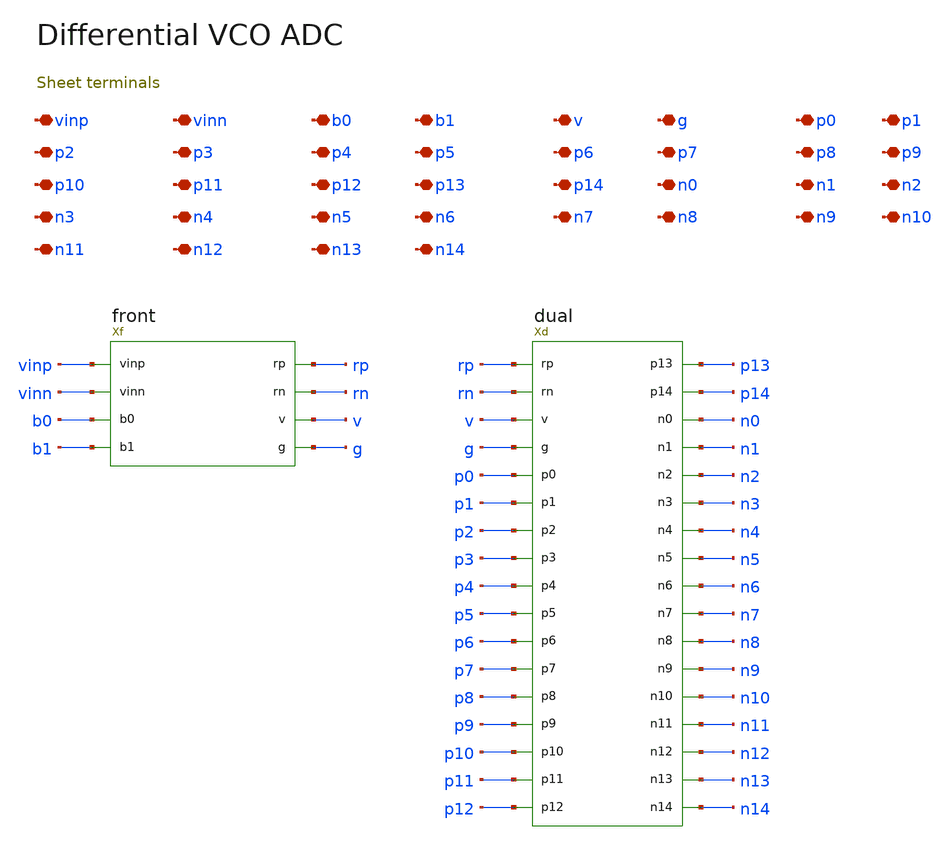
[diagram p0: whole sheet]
** sch_path: review/xschem/adc_analog.sch
**.subckt adc_analog vinp vinn b0 b1 v g p0 p1 p2 p3 p4 p5 p6 p7 p8 p9 p10 p11 p12 p13 p14 n0 n1 n2
*+ n3 n4 n5 n6 n7 n8 n9 n10 n11 n12 n13 n14
*.iopin vinp
*.iopin vinn
*.iopin b0
*.iopin b1
*.iopin v
*.iopin g
*.iopin p0
*.iopin p1
*.iopin p2
*.iopin p3
*.iopin p4
*.iopin p5
*.iopin p6
*.iopin p7
*.iopin p8
*.iopin p9
*.iopin p10
*.iopin p11
*.iopin p12
*.iopin p13
*.iopin p14
*.iopin n0
*.iopin n1
*.iopin n2
*.iopin n3
*.iopin n4
*.iopin n5
*.iopin n6
*.iopin n7
*.iopin n8
*.iopin n9
*.iopin n10
*.iopin n11
*.iopin n12
*.iopin n13
*.iopin n14
Xf vinp vinn b0 b1 rp rn v g front
Xd rp rn v g p0 p1 p2 p3 p4 p5 p6 p7 p8 p9 p10 p11 p12 p13 p14 n0 n1 n2 n3 n4 n5 n6 n7 n8 n9 n10 n11
+ n12 n13 n14 dual
**.ends

* expanding   symbol:  front.sym # of pins=8
** sym_path: review/xschem/front.sym
** sch_path: review/xschem/front.sch
.subckt front vinp vinn b0 b1 rp rn v g
*.iopin vinp
*.iopin vinn
*.iopin b0
*.iopin b1
*.iopin rp
*.iopin rn
*.iopin v
*.iopin g
Xbias b0 b1 vb g4 g15 g20 v g bias
Xtailp sp vb g4 g15 g20 v tail
Xtailn sn vb g4 g15 g20 v tail
XMinp0 rp vinn sp sp sky130_fd_pr__pfet_01v8_lvt L=1 W=6 nf=1 ad='int((1 + 1)/2) * 6 / 1 * 0.29' as='int((1 + 2)/2) * 6 / 1 * 0.29'
+ pd='2*int((1 + 1)/2) * (6 / 1 + 0.29)' ps='2*int((1 + 2)/2) * (6 / 1 + 0.29)' nrd='0.29 / 6 ' nrs='0.29 / 6 '
+ sa=0 sb=0 sd=0 mult=1 m=1
XMinp1 rp vinn sp sp sky130_fd_pr__pfet_01v8_lvt L=1 W=6 nf=1 ad='int((1 + 1)/2) * 6 / 1 * 0.29' as='int((1 + 2)/2) * 6 / 1 * 0.29'
+ pd='2*int((1 + 1)/2) * (6 / 1 + 0.29)' ps='2*int((1 + 2)/2) * (6 / 1 + 0.29)' nrd='0.29 / 6 ' nrs='0.29 / 6 '
+ sa=0 sb=0 sd=0 mult=1 m=1
XMinp2 rp vinn sp sp sky130_fd_pr__pfet_01v8_lvt L=1 W=6 nf=1 ad='int((1 + 1)/2) * 6 / 1 * 0.29' as='int((1 + 2)/2) * 6 / 1 * 0.29'
+ pd='2*int((1 + 1)/2) * (6 / 1 + 0.29)' ps='2*int((1 + 2)/2) * (6 / 1 + 0.29)' nrd='0.29 / 6 ' nrs='0.29 / 6 '
+ sa=0 sb=0 sd=0 mult=1 m=1
XMinp3 rp vinn sp sp sky130_fd_pr__pfet_01v8_lvt L=1 W=6 nf=1 ad='int((1 + 1)/2) * 6 / 1 * 0.29' as='int((1 + 2)/2) * 6 / 1 * 0.29'
+ pd='2*int((1 + 1)/2) * (6 / 1 + 0.29)' ps='2*int((1 + 2)/2) * (6 / 1 + 0.29)' nrd='0.29 / 6 ' nrs='0.29 / 6 '
+ sa=0 sb=0 sd=0 mult=1 m=1
XMinn0 rn vinp sn sn sky130_fd_pr__pfet_01v8_lvt L=1 W=6 nf=1 ad='int((1 + 1)/2) * 6 / 1 * 0.29' as='int((1 + 2)/2) * 6 / 1 * 0.29'
+ pd='2*int((1 + 1)/2) * (6 / 1 + 0.29)' ps='2*int((1 + 2)/2) * (6 / 1 + 0.29)' nrd='0.29 / 6 ' nrs='0.29 / 6 '
+ sa=0 sb=0 sd=0 mult=1 m=1
XMinn1 rn vinp sn sn sky130_fd_pr__pfet_01v8_lvt L=1 W=6 nf=1 ad='int((1 + 1)/2) * 6 / 1 * 0.29' as='int((1 + 2)/2) * 6 / 1 * 0.29'
+ pd='2*int((1 + 1)/2) * (6 / 1 + 0.29)' ps='2*int((1 + 2)/2) * (6 / 1 + 0.29)' nrd='0.29 / 6 ' nrs='0.29 / 6 '
+ sa=0 sb=0 sd=0 mult=1 m=1
XMinn2 rn vinp sn sn sky130_fd_pr__pfet_01v8_lvt L=1 W=6 nf=1 ad='int((1 + 1)/2) * 6 / 1 * 0.29' as='int((1 + 2)/2) * 6 / 1 * 0.29'
+ pd='2*int((1 + 1)/2) * (6 / 1 + 0.29)' ps='2*int((1 + 2)/2) * (6 / 1 + 0.29)' nrd='0.29 / 6 ' nrs='0.29 / 6 '
+ sa=0 sb=0 sd=0 mult=1 m=1
XMinn3 rn vinp sn sn sky130_fd_pr__pfet_01v8_lvt L=1 W=6 nf=1 ad='int((1 + 1)/2) * 6 / 1 * 0.29' as='int((1 + 2)/2) * 6 / 1 * 0.29'
+ pd='2*int((1 + 1)/2) * (6 / 1 + 0.29)' ps='2*int((1 + 2)/2) * (6 / 1 + 0.29)' nrd='0.29 / 6 ' nrs='0.29 / 6 '
+ sa=0 sb=0 sd=0 mult=1 m=1
XRr0 sp mid g sky130_fd_pr__res_high_po_0p69 L=80 mult=1 m=1
XRr1 mid sn g sky130_fd_pr__res_high_po_0p69 L=80 mult=1 m=1
XCcapP rp g sky130_fd_pr__cap_mim_m3_1 W=21.8 L=21.8 MF=1 m=1
XCcapN rn g sky130_fd_pr__cap_mim_m3_1 W=21.8 L=21.8 MF=1 m=1
.ends


* expanding   symbol:  dual.sym # of pins=34
** sym_path: review/xschem/dual.sym
** sch_path: review/xschem/dual.sch
.subckt dual rp rn v g p0 p1 p2 p3 p4 p5 p6 p7 p8 p9 p10 p11 p12 p13 p14 n0 n1 n2 n3 n4 n5 n6 n7 n8
+ n9 n10 n11 n12 n13 n14
*.iopin rp
*.iopin rn
*.iopin v
*.iopin g
*.iopin p0
*.iopin p1
*.iopin p2
*.iopin p3
*.iopin p4
*.iopin p5
*.iopin p6
*.iopin p7
*.iopin p8
*.iopin p9
*.iopin p10
*.iopin p11
*.iopin p12
*.iopin p13
*.iopin p14
*.iopin n0
*.iopin n1
*.iopin n2
*.iopin n3
*.iopin n4
*.iopin n5
*.iopin n6
*.iopin n7
*.iopin n8
*.iopin n9
*.iopin n10
*.iopin n11
*.iopin n12
*.iopin n13
*.iopin n14
Xp rp v g p0 p1 p2 p3 p4 p5 p6 p7 p8 p9 p10 p11 p12 p13 p14 ring
Xn rn v g n0 n1 n2 n3 n4 n5 n6 n7 n8 n9 n10 n11 n12 n13 n14 ring
.ends


* expanding   symbol:  bias.sym # of pins=8
** sym_path: review/xschem/bias.sym
** sch_path: review/xschem/bias.sch
.subckt bias b0 b1 vb g4 g15 g20 v g
*.iopin b0
*.iopin b1
*.iopin vb
*.iopin g4
*.iopin g15
*.iopin g20
*.iopin v
*.iopin g
Xreference vb v g beta_ref
XMi0p nb0 b0 v v sky130_fd_pr__pfet_01v8 L=.15 W=.84 nf=1 ad='int((nf+1)/2) * W/nf * 0.29' as='int((nf+2)/2) * W/nf * 0.29'
+ pd='2*int((nf+1)/2) * (W/nf + 0.29)' ps='2*int((nf+2)/2) * (W/nf + 0.29)' nrd='0.29 / W' nrs='0.29 / W'
+ sa=0 sb=0 sd=0 mult=1 m=1
XMi0n nb0 b0 g g sky130_fd_pr__nfet_01v8 L=.15 W=.42 nf=1 ad='int((1 + 1)/2) * .42 / 1 * 0.29' as='int((1 + 2)/2) * .42 / 1 * 0.29'
+ pd='2*int((1 + 1)/2) * (.42 / 1 + 0.29)' ps='2*int((1 + 2)/2) * (.42 / 1 + 0.29)' nrd='0.29 / .42 ' nrs='0.29 / .42 '
+ sa=0 sb=0 sd=0 mult=1 m=1
XMi1p nb1 b1 v v sky130_fd_pr__pfet_01v8 L=.15 W=.84 nf=1 ad='int((nf+1)/2) * W/nf * 0.29' as='int((nf+2)/2) * W/nf * 0.29'
+ pd='2*int((nf+1)/2) * (W/nf + 0.29)' ps='2*int((nf+2)/2) * (W/nf + 0.29)' nrd='0.29 / W' nrs='0.29 / W'
+ sa=0 sb=0 sd=0 mult=1 m=1
XMi1n nb1 b1 g g sky130_fd_pr__nfet_01v8 L=.15 W=.42 nf=1 ad='int((1 + 1)/2) * .42 / 1 * 0.29' as='int((1 + 2)/2) * .42 / 1 * 0.29'
+ pd='2*int((1 + 1)/2) * (.42 / 1 + 0.29)' ps='2*int((1 + 2)/2) * (.42 / 1 + 0.29)' nrd='0.29 / .42 ' nrs='0.29 / .42 '
+ sa=0 sb=0 sd=0 mult=1 m=1
Xonlylow nb0 b1 off4 v g nor2
XMi4p en4 off4 v v sky130_fd_pr__pfet_01v8 L=.15 W=.84 nf=1 ad='int((nf+1)/2) * W/nf * 0.29' as='int((nf+2)/2) * W/nf * 0.29'
+ pd='2*int((nf+1)/2) * (W/nf + 0.29)' ps='2*int((nf+2)/2) * (W/nf + 0.29)' nrd='0.29 / W' nrs='0.29 / W'
+ sa=0 sb=0 sd=0 mult=1 m=1
XMi4n en4 off4 g g sky130_fd_pr__nfet_01v8 L=.15 W=.42 nf=1 ad='int((1 + 1)/2) * .42 / 1 * 0.29' as='int((1 + 2)/2) * .42 / 1 * 0.29'
+ pd='2*int((1 + 1)/2) * (.42 / 1 + 0.29)' ps='2*int((1 + 2)/2) * (.42 / 1 + 0.29)' nrd='0.29 / .42 ' nrs='0.29 / .42 '
+ sa=0 sb=0 sd=0 mult=1 m=1
Xboth nb0 nb1 en20 v g nor2
Xzero b0 b1 zero v g nor2
Xdiff zero en20 off15 v g nor2
XMi15p en15 off15 v v sky130_fd_pr__pfet_01v8 L=.15 W=.84 nf=1 ad='int((nf+1)/2) * W/nf * 0.29' as='int((nf+2)/2) * W/nf * 0.29'
+ pd='2*int((nf+1)/2) * (W/nf + 0.29)' ps='2*int((nf+2)/2) * (W/nf + 0.29)' nrd='0.29 / W' nrs='0.29 / W'
+ sa=0 sb=0 sd=0 mult=1 m=1
XMi15n en15 off15 g g sky130_fd_pr__nfet_01v8 L=.15 W=.42 nf=1 ad='int((1 + 1)/2) * .42 / 1 * 0.29' as='int((1 + 2)/2) * .42 / 1 * 0.29'
+ pd='2*int((1 + 1)/2) * (.42 / 1 + 0.29)' ps='2*int((1 + 2)/2) * (.42 / 1 + 0.29)' nrd='0.29 / .42 ' nrs='0.29 / .42 '
+ sa=0 sb=0 sd=0 mult=1 m=1
XMi20p off20 en20 v v sky130_fd_pr__pfet_01v8 L=.15 W=.84 nf=1 ad='int((nf+1)/2) * W/nf * 0.29' as='int((nf+2)/2) * W/nf * 0.29'
+ pd='2*int((nf+1)/2) * (W/nf + 0.29)' ps='2*int((nf+2)/2) * (W/nf + 0.29)' nrd='0.29 / W' nrs='0.29 / W'
+ sa=0 sb=0 sd=0 mult=1 m=1
XMi20n off20 en20 g g sky130_fd_pr__nfet_01v8 L=.15 W=.42 nf=1 ad='int((1 + 1)/2) * .42 / 1 * 0.29' as='int((1 + 2)/2) * .42 / 1 * 0.29'
+ pd='2*int((1 + 1)/2) * (.42 / 1 + 0.29)' ps='2*int((1 + 2)/2) * (.42 / 1 + 0.29)' nrd='0.29 / .42 ' nrs='0.29 / .42 '
+ sa=0 sb=0 sd=0 mult=1 m=1
Xsw4 en4 off4 vb g4 v g tailgate
Xsw15 en15 off15 vb g15 v g tailgate
Xsw20 en20 off20 vb g20 v g tailgate
.ends


* expanding   symbol:  tail.sym # of pins=6
** sym_path: review/xschem/tail.sym
** sch_path: review/xschem/tail.sch
.subckt tail s vb g4 g15 g20 v
*.iopin s
*.iopin vb
*.iopin g4
*.iopin g15
*.iopin g20
*.iopin v
XMone s vb v v sky130_fd_pr__pfet_01v8 L=2 W=1 nf=1 ad='int((nf+1)/2) * W/nf * 0.29' as='int((nf+2)/2) * W/nf * 0.29'
+ pd='2*int((nf+1)/2) * (W/nf + 0.29)' ps='2*int((nf+2)/2) * (W/nf + 0.29)' nrd='0.29 / W' nrs='0.29 / W'
+ sa=0 sb=0 sd=0 mult=1 m=1
Xunits4 s g4 v units4
Xunits15 s g15 v units15
Xunits20 s g20 v units20
.ends


* expanding   symbol:  ring.sym # of pins=18
** sym_path: review/xschem/ring.sym
** sch_path: review/xschem/ring.sch
.subckt ring rail v g t0 t1 t2 t3 t4 t5 t6 t7 t8 t9 t10 t11 t12 t13 t14
*.iopin rail
*.iopin v
*.iopin g
*.iopin t0
*.iopin t1
*.iopin t2
*.iopin t3
*.iopin t4
*.iopin t5
*.iopin t6
*.iopin t7
*.iopin t8
*.iopin t9
*.iopin t10
*.iopin t11
*.iopin t12
*.iopin t13
*.iopin t14
Xbank rail v g oa0 ob0 oa1 ob1 oa2 ob2 oa3 ob3 oa4 ob4 oa5 ob5 oa6 ob6 oa7 ob7 oa8 ob8 oa9 ob9 oa10
+ ob10 oa11 ob11 oa12 ob12 oa13 ob13 oa14 ob14 bank
Xl0 oa0 ob0 t0 v g cvsl
Xl1 oa1 ob1 t1 v g cvsl
Xl2 oa2 ob2 t2 v g cvsl
Xl3 oa3 ob3 t3 v g cvsl
Xl4 oa4 ob4 t4 v g cvsl
Xl5 oa5 ob5 t5 v g cvsl
Xl6 oa6 ob6 t6 v g cvsl
Xl7 oa7 ob7 t7 v g cvsl
Xl8 oa8 ob8 t8 v g cvsl
Xl9 oa9 ob9 t9 v g cvsl
Xl10 oa10 ob10 t10 v g cvsl
Xl11 oa11 ob11 t11 v g cvsl
Xl12 oa12 ob12 t12 v g cvsl
Xl13 oa13 ob13 t13 v g cvsl
Xl14 oa14 ob14 t14 v g cvsl
.ends


* expanding   symbol:  beta_ref.sym # of pins=3
** sym_path: review/xschem/beta_ref.sym
** sch_path: review/xschem/beta_ref.sch
.subckt beta_ref vb v g
*.iopin vb
*.iopin v
*.iopin g
XMp0 vb vb v v sky130_fd_pr__pfet_01v8 L=2 W=2 nf=1 ad='int((nf+1)/2) * W/nf * 0.29' as='int((nf+2)/2) * W/nf * 0.29'
+ pd='2*int((nf+1)/2) * (W/nf + 0.29)' ps='2*int((nf+2)/2) * (W/nf + 0.29)' nrd='0.29 / W' nrs='0.29 / W'
+ sa=0 sb=0 sd=0 mult=1 m=1
XMn0 vn vn g g sky130_fd_pr__nfet_01v8 L=2 W=2 nf=1 ad='int((1 + 1)/2) * 2 / 1 * 0.29' as='int((1 + 2)/2) * 2 / 1 * 0.29'
+ pd='2*int((1 + 1)/2) * (2 / 1 + 0.29)' ps='2*int((1 + 2)/2) * (2 / 1 + 0.29)' nrd='0.29 / 2 ' nrs='0.29 / 2 '
+ sa=0 sb=0 sd=0 mult=1 m=1
XMp1 vn vb v v sky130_fd_pr__pfet_01v8 L=2 W=2 nf=1 ad='int((nf+1)/2) * W/nf * 0.29' as='int((nf+2)/2) * W/nf * 0.29'
+ pd='2*int((nf+1)/2) * (W/nf + 0.29)' ps='2*int((nf+2)/2) * (W/nf + 0.29)' nrd='0.29 / W' nrs='0.29 / W'
+ sa=0 sb=0 sd=0 mult=1 m=1
XMn1 vb vn rs g sky130_fd_pr__nfet_01v8 L=2 W=8 nf=1 ad='int((1 + 1)/2) * 8 / 1 * 0.29' as='int((1 + 2)/2) * 8 / 1 * 0.29'
+ pd='2*int((1 + 1)/2) * (8 / 1 + 0.29)' ps='2*int((1 + 2)/2) * (8 / 1 + 0.29)' nrd='0.29 / 8 ' nrs='0.29 / 8 '
+ sa=0 sb=0 sd=0 mult=1 m=1
XRref0 rs refmid g sky130_fd_pr__res_high_po_0p69 L=97.1 mult=1 m=1
XRref1 refmid g g sky130_fd_pr__res_high_po_0p69 L=97.1 mult=1 m=1
XMweak kick g v v sky130_fd_pr__pfet_01v8 L=12 W=.42 nf=1 ad='int((nf+1)/2) * W/nf * 0.29' as='int((nf+2)/2) * W/nf * 0.29'
+ pd='2*int((nf+1)/2) * (W/nf + 0.29)' ps='2*int((nf+2)/2) * (W/nf + 0.29)' nrd='0.29 / W' nrs='0.29 / W'
+ sa=0 sb=0 sd=0 mult=1 m=1
XMsense kick vn g g sky130_fd_pr__nfet_01v8_lvt L=.15 W=5 nf=1 ad='int((1 + 1)/2) * 5 / 1 * 0.29' as='int((1 + 2)/2) * 5 / 1 * 0.29'
+ pd='2*int((1 + 1)/2) * (5 / 1 + 0.29)' ps='2*int((1 + 2)/2) * (5 / 1 + 0.29)' nrd='0.29 / 5 ' nrs='0.29 / 5 '
+ sa=0 sb=0 sd=0 mult=1 m=1
XMkick vb kick g g sky130_fd_pr__nfet_01v8 L=1 W=.5 nf=1 ad='int((1 + 1)/2) * .5 / 1 * 0.29' as='int((1 + 2)/2) * .5 / 1 * 0.29'
+ pd='2*int((1 + 1)/2) * (.5 / 1 + 0.29)' ps='2*int((1 + 2)/2) * (.5 / 1 + 0.29)' nrd='0.29 / .5 ' nrs='0.29 / .5 '
+ sa=0 sb=0 sd=0 mult=1 m=1
.ends


* expanding   symbol:  nor2.sym # of pins=5
** sym_path: review/xschem/nor2.sym
** sch_path: review/xschem/nor2.sch
.subckt nor2 a b y v g
*.iopin a
*.iopin b
*.iopin y
*.iopin v
*.iopin g
XMp0 mid a v v sky130_fd_pr__pfet_01v8 L=.15 W=.84 nf=1 ad='int((nf+1)/2) * W/nf * 0.29' as='int((nf+2)/2) * W/nf * 0.29'
+ pd='2*int((nf+1)/2) * (W/nf + 0.29)' ps='2*int((nf+2)/2) * (W/nf + 0.29)' nrd='0.29 / W' nrs='0.29 / W'
+ sa=0 sb=0 sd=0 mult=1 m=1
XMp1 y b mid v sky130_fd_pr__pfet_01v8 L=.15 W=.84 nf=1 ad='int((nf+1)/2) * W/nf * 0.29' as='int((nf+2)/2) * W/nf * 0.29'
+ pd='2*int((nf+1)/2) * (W/nf + 0.29)' ps='2*int((nf+2)/2) * (W/nf + 0.29)' nrd='0.29 / W' nrs='0.29 / W'
+ sa=0 sb=0 sd=0 mult=1 m=1
XMn0 y a g g sky130_fd_pr__nfet_01v8 L=.15 W=.42 nf=1 ad='int((1 + 1)/2) * .42 / 1 * 0.29' as='int((1 + 2)/2) * .42 / 1 * 0.29'
+ pd='2*int((1 + 1)/2) * (.42 / 1 + 0.29)' ps='2*int((1 + 2)/2) * (.42 / 1 + 0.29)' nrd='0.29 / .42 ' nrs='0.29 / .42 '
+ sa=0 sb=0 sd=0 mult=1 m=1
XMn1 y b g g sky130_fd_pr__nfet_01v8 L=.15 W=.42 nf=1 ad='int((1 + 1)/2) * .42 / 1 * 0.29' as='int((1 + 2)/2) * .42 / 1 * 0.29'
+ pd='2*int((1 + 1)/2) * (.42 / 1 + 0.29)' ps='2*int((1 + 2)/2) * (.42 / 1 + 0.29)' nrd='0.29 / .42 ' nrs='0.29 / .42 '
+ sa=0 sb=0 sd=0 mult=1 m=1
.ends


* expanding   symbol:  tailgate.sym # of pins=6
** sym_path: review/xschem/tailgate.sym
** sch_path: review/xschem/tailgate.sch
.subckt tailgate en enb vb out v g
*.iopin en
*.iopin enb
*.iopin vb
*.iopin out
*.iopin v
*.iopin g
XMonp out enb vb v sky130_fd_pr__pfet_01v8 L=.15 W=.84 nf=1 ad='int((nf+1)/2) * W/nf * 0.29' as='int((nf+2)/2) * W/nf * 0.29'
+ pd='2*int((nf+1)/2) * (W/nf + 0.29)' ps='2*int((nf+2)/2) * (W/nf + 0.29)' nrd='0.29 / W' nrs='0.29 / W'
+ sa=0 sb=0 sd=0 mult=1 m=1
XMonn out en vb g sky130_fd_pr__nfet_01v8 L=.15 W=.42 nf=1 ad='int((1 + 1)/2) * .42 / 1 * 0.29' as='int((1 + 2)/2) * .42 / 1 * 0.29'
+ pd='2*int((1 + 1)/2) * (.42 / 1 + 0.29)' ps='2*int((1 + 2)/2) * (.42 / 1 + 0.29)' nrd='0.29 / .42 ' nrs='0.29 / .42 '
+ sa=0 sb=0 sd=0 mult=1 m=1
XMoff out en v v sky130_fd_pr__pfet_01v8 L=.15 W=.84 nf=1 ad='int((nf+1)/2) * W/nf * 0.29' as='int((nf+2)/2) * W/nf * 0.29'
+ pd='2*int((nf+1)/2) * (W/nf + 0.29)' ps='2*int((nf+2)/2) * (W/nf + 0.29)' nrd='0.29 / W' nrs='0.29 / W'
+ sa=0 sb=0 sd=0 mult=1 m=1
.ends


* expanding   symbol:  units4.sym # of pins=3
** sym_path: review/xschem/units4.sym
** sch_path: review/xschem/units4.sch
.subckt units4 s control v
*.iopin s
*.iopin control
*.iopin v
XMg4_1 s control v v sky130_fd_pr__pfet_01v8 L=2 W=1 nf=1 ad='int((nf+1)/2) * W/nf * 0.29' as='int((nf+2)/2) * W/nf * 0.29'
+ pd='2*int((nf+1)/2) * (W/nf + 0.29)' ps='2*int((nf+2)/2) * (W/nf + 0.29)' nrd='0.29 / W' nrs='0.29 / W'
+ sa=0 sb=0 sd=0 mult=1 m=1
XMg4_2 s control v v sky130_fd_pr__pfet_01v8 L=2 W=1 nf=1 ad='int((nf+1)/2) * W/nf * 0.29' as='int((nf+2)/2) * W/nf * 0.29'
+ pd='2*int((nf+1)/2) * (W/nf + 0.29)' ps='2*int((nf+2)/2) * (W/nf + 0.29)' nrd='0.29 / W' nrs='0.29 / W'
+ sa=0 sb=0 sd=0 mult=1 m=1
XMg4_3 s control v v sky130_fd_pr__pfet_01v8 L=2 W=1 nf=1 ad='int((nf+1)/2) * W/nf * 0.29' as='int((nf+2)/2) * W/nf * 0.29'
+ pd='2*int((nf+1)/2) * (W/nf + 0.29)' ps='2*int((nf+2)/2) * (W/nf + 0.29)' nrd='0.29 / W' nrs='0.29 / W'
+ sa=0 sb=0 sd=0 mult=1 m=1
XMg4_4 s control v v sky130_fd_pr__pfet_01v8 L=2 W=1 nf=1 ad='int((nf+1)/2) * W/nf * 0.29' as='int((nf+2)/2) * W/nf * 0.29'
+ pd='2*int((nf+1)/2) * (W/nf + 0.29)' ps='2*int((nf+2)/2) * (W/nf + 0.29)' nrd='0.29 / W' nrs='0.29 / W'
+ sa=0 sb=0 sd=0 mult=1 m=1
.ends


* expanding   symbol:  units15.sym # of pins=3
** sym_path: review/xschem/units15.sym
** sch_path: review/xschem/units15.sch
.subckt units15 s control v
*.iopin s
*.iopin control
*.iopin v
XMg15_1 s control v v sky130_fd_pr__pfet_01v8 L=2 W=1 nf=1 ad='int((nf+1)/2) * W/nf * 0.29' as='int((nf+2)/2) * W/nf * 0.29'
+ pd='2*int((nf+1)/2) * (W/nf + 0.29)' ps='2*int((nf+2)/2) * (W/nf + 0.29)' nrd='0.29 / W' nrs='0.29 / W'
+ sa=0 sb=0 sd=0 mult=1 m=1
XMg15_2 s control v v sky130_fd_pr__pfet_01v8 L=2 W=1 nf=1 ad='int((nf+1)/2) * W/nf * 0.29' as='int((nf+2)/2) * W/nf * 0.29'
+ pd='2*int((nf+1)/2) * (W/nf + 0.29)' ps='2*int((nf+2)/2) * (W/nf + 0.29)' nrd='0.29 / W' nrs='0.29 / W'
+ sa=0 sb=0 sd=0 mult=1 m=1
XMg15_3 s control v v sky130_fd_pr__pfet_01v8 L=2 W=1 nf=1 ad='int((nf+1)/2) * W/nf * 0.29' as='int((nf+2)/2) * W/nf * 0.29'
+ pd='2*int((nf+1)/2) * (W/nf + 0.29)' ps='2*int((nf+2)/2) * (W/nf + 0.29)' nrd='0.29 / W' nrs='0.29 / W'
+ sa=0 sb=0 sd=0 mult=1 m=1
XMg15_4 s control v v sky130_fd_pr__pfet_01v8 L=2 W=1 nf=1 ad='int((nf+1)/2) * W/nf * 0.29' as='int((nf+2)/2) * W/nf * 0.29'
+ pd='2*int((nf+1)/2) * (W/nf + 0.29)' ps='2*int((nf+2)/2) * (W/nf + 0.29)' nrd='0.29 / W' nrs='0.29 / W'
+ sa=0 sb=0 sd=0 mult=1 m=1
XMg15_5 s control v v sky130_fd_pr__pfet_01v8 L=2 W=1 nf=1 ad='int((nf+1)/2) * W/nf * 0.29' as='int((nf+2)/2) * W/nf * 0.29'
+ pd='2*int((nf+1)/2) * (W/nf + 0.29)' ps='2*int((nf+2)/2) * (W/nf + 0.29)' nrd='0.29 / W' nrs='0.29 / W'
+ sa=0 sb=0 sd=0 mult=1 m=1
XMg15_6 s control v v sky130_fd_pr__pfet_01v8 L=2 W=1 nf=1 ad='int((nf+1)/2) * W/nf * 0.29' as='int((nf+2)/2) * W/nf * 0.29'
+ pd='2*int((nf+1)/2) * (W/nf + 0.29)' ps='2*int((nf+2)/2) * (W/nf + 0.29)' nrd='0.29 / W' nrs='0.29 / W'
+ sa=0 sb=0 sd=0 mult=1 m=1
XMg15_7 s control v v sky130_fd_pr__pfet_01v8 L=2 W=1 nf=1 ad='int((nf+1)/2) * W/nf * 0.29' as='int((nf+2)/2) * W/nf * 0.29'
+ pd='2*int((nf+1)/2) * (W/nf + 0.29)' ps='2*int((nf+2)/2) * (W/nf + 0.29)' nrd='0.29 / W' nrs='0.29 / W'
+ sa=0 sb=0 sd=0 mult=1 m=1
XMg15_8 s control v v sky130_fd_pr__pfet_01v8 L=2 W=1 nf=1 ad='int((nf+1)/2) * W/nf * 0.29' as='int((nf+2)/2) * W/nf * 0.29'
+ pd='2*int((nf+1)/2) * (W/nf + 0.29)' ps='2*int((nf+2)/2) * (W/nf + 0.29)' nrd='0.29 / W' nrs='0.29 / W'
+ sa=0 sb=0 sd=0 mult=1 m=1
XMg15_9 s control v v sky130_fd_pr__pfet_01v8 L=2 W=1 nf=1 ad='int((nf+1)/2) * W/nf * 0.29' as='int((nf+2)/2) * W/nf * 0.29'
+ pd='2*int((nf+1)/2) * (W/nf + 0.29)' ps='2*int((nf+2)/2) * (W/nf + 0.29)' nrd='0.29 / W' nrs='0.29 / W'
+ sa=0 sb=0 sd=0 mult=1 m=1
XMg15_10 s control v v sky130_fd_pr__pfet_01v8 L=2 W=1 nf=1 ad='int((nf+1)/2) * W/nf * 0.29' as='int((nf+2)/2) * W/nf * 0.29'
+ pd='2*int((nf+1)/2) * (W/nf + 0.29)' ps='2*int((nf+2)/2) * (W/nf + 0.29)' nrd='0.29 / W' nrs='0.29 / W'
+ sa=0 sb=0 sd=0 mult=1 m=1
XMg15_11 s control v v sky130_fd_pr__pfet_01v8 L=2 W=1 nf=1 ad='int((nf+1)/2) * W/nf * 0.29' as='int((nf+2)/2) * W/nf * 0.29'
+ pd='2*int((nf+1)/2) * (W/nf + 0.29)' ps='2*int((nf+2)/2) * (W/nf + 0.29)' nrd='0.29 / W' nrs='0.29 / W'
+ sa=0 sb=0 sd=0 mult=1 m=1
XMg15_12 s control v v sky130_fd_pr__pfet_01v8 L=2 W=1 nf=1 ad='int((nf+1)/2) * W/nf * 0.29' as='int((nf+2)/2) * W/nf * 0.29'
+ pd='2*int((nf+1)/2) * (W/nf + 0.29)' ps='2*int((nf+2)/2) * (W/nf + 0.29)' nrd='0.29 / W' nrs='0.29 / W'
+ sa=0 sb=0 sd=0 mult=1 m=1
XMg15_13 s control v v sky130_fd_pr__pfet_01v8 L=2 W=1 nf=1 ad='int((nf+1)/2) * W/nf * 0.29' as='int((nf+2)/2) * W/nf * 0.29'
+ pd='2*int((nf+1)/2) * (W/nf + 0.29)' ps='2*int((nf+2)/2) * (W/nf + 0.29)' nrd='0.29 / W' nrs='0.29 / W'
+ sa=0 sb=0 sd=0 mult=1 m=1
XMg15_14 s control v v sky130_fd_pr__pfet_01v8 L=2 W=1 nf=1 ad='int((nf+1)/2) * W/nf * 0.29' as='int((nf+2)/2) * W/nf * 0.29'
+ pd='2*int((nf+1)/2) * (W/nf + 0.29)' ps='2*int((nf+2)/2) * (W/nf + 0.29)' nrd='0.29 / W' nrs='0.29 / W'
+ sa=0 sb=0 sd=0 mult=1 m=1
XMg15_15 s control v v sky130_fd_pr__pfet_01v8 L=2 W=1 nf=1 ad='int((nf+1)/2) * W/nf * 0.29' as='int((nf+2)/2) * W/nf * 0.29'
+ pd='2*int((nf+1)/2) * (W/nf + 0.29)' ps='2*int((nf+2)/2) * (W/nf + 0.29)' nrd='0.29 / W' nrs='0.29 / W'
+ sa=0 sb=0 sd=0 mult=1 m=1
.ends


* expanding   symbol:  units20.sym # of pins=3
** sym_path: review/xschem/units20.sym
** sch_path: review/xschem/units20.sch
.subckt units20 s control v
*.iopin s
*.iopin control
*.iopin v
XMg20_1 s control v v sky130_fd_pr__pfet_01v8 L=2 W=1 nf=1 ad='int((nf+1)/2) * W/nf * 0.29' as='int((nf+2)/2) * W/nf * 0.29'
+ pd='2*int((nf+1)/2) * (W/nf + 0.29)' ps='2*int((nf+2)/2) * (W/nf + 0.29)' nrd='0.29 / W' nrs='0.29 / W'
+ sa=0 sb=0 sd=0 mult=1 m=1
XMg20_2 s control v v sky130_fd_pr__pfet_01v8 L=2 W=1 nf=1 ad='int((nf+1)/2) * W/nf * 0.29' as='int((nf+2)/2) * W/nf * 0.29'
+ pd='2*int((nf+1)/2) * (W/nf + 0.29)' ps='2*int((nf+2)/2) * (W/nf + 0.29)' nrd='0.29 / W' nrs='0.29 / W'
+ sa=0 sb=0 sd=0 mult=1 m=1
XMg20_3 s control v v sky130_fd_pr__pfet_01v8 L=2 W=1 nf=1 ad='int((nf+1)/2) * W/nf * 0.29' as='int((nf+2)/2) * W/nf * 0.29'
+ pd='2*int((nf+1)/2) * (W/nf + 0.29)' ps='2*int((nf+2)/2) * (W/nf + 0.29)' nrd='0.29 / W' nrs='0.29 / W'
+ sa=0 sb=0 sd=0 mult=1 m=1
XMg20_4 s control v v sky130_fd_pr__pfet_01v8 L=2 W=1 nf=1 ad='int((nf+1)/2) * W/nf * 0.29' as='int((nf+2)/2) * W/nf * 0.29'
+ pd='2*int((nf+1)/2) * (W/nf + 0.29)' ps='2*int((nf+2)/2) * (W/nf + 0.29)' nrd='0.29 / W' nrs='0.29 / W'
+ sa=0 sb=0 sd=0 mult=1 m=1
XMg20_5 s control v v sky130_fd_pr__pfet_01v8 L=2 W=1 nf=1 ad='int((nf+1)/2) * W/nf * 0.29' as='int((nf+2)/2) * W/nf * 0.29'
+ pd='2*int((nf+1)/2) * (W/nf + 0.29)' ps='2*int((nf+2)/2) * (W/nf + 0.29)' nrd='0.29 / W' nrs='0.29 / W'
+ sa=0 sb=0 sd=0 mult=1 m=1
XMg20_6 s control v v sky130_fd_pr__pfet_01v8 L=2 W=1 nf=1 ad='int((nf+1)/2) * W/nf * 0.29' as='int((nf+2)/2) * W/nf * 0.29'
+ pd='2*int((nf+1)/2) * (W/nf + 0.29)' ps='2*int((nf+2)/2) * (W/nf + 0.29)' nrd='0.29 / W' nrs='0.29 / W'
+ sa=0 sb=0 sd=0 mult=1 m=1
XMg20_7 s control v v sky130_fd_pr__pfet_01v8 L=2 W=1 nf=1 ad='int((nf+1)/2) * W/nf * 0.29' as='int((nf+2)/2) * W/nf * 0.29'
+ pd='2*int((nf+1)/2) * (W/nf + 0.29)' ps='2*int((nf+2)/2) * (W/nf + 0.29)' nrd='0.29 / W' nrs='0.29 / W'
+ sa=0 sb=0 sd=0 mult=1 m=1
XMg20_8 s control v v sky130_fd_pr__pfet_01v8 L=2 W=1 nf=1 ad='int((nf+1)/2) * W/nf * 0.29' as='int((nf+2)/2) * W/nf * 0.29'
+ pd='2*int((nf+1)/2) * (W/nf + 0.29)' ps='2*int((nf+2)/2) * (W/nf + 0.29)' nrd='0.29 / W' nrs='0.29 / W'
+ sa=0 sb=0 sd=0 mult=1 m=1
XMg20_9 s control v v sky130_fd_pr__pfet_01v8 L=2 W=1 nf=1 ad='int((nf+1)/2) * W/nf * 0.29' as='int((nf+2)/2) * W/nf * 0.29'
+ pd='2*int((nf+1)/2) * (W/nf + 0.29)' ps='2*int((nf+2)/2) * (W/nf + 0.29)' nrd='0.29 / W' nrs='0.29 / W'
+ sa=0 sb=0 sd=0 mult=1 m=1
XMg20_10 s control v v sky130_fd_pr__pfet_01v8 L=2 W=1 nf=1 ad='int((nf+1)/2) * W/nf * 0.29' as='int((nf+2)/2) * W/nf * 0.29'
+ pd='2*int((nf+1)/2) * (W/nf + 0.29)' ps='2*int((nf+2)/2) * (W/nf + 0.29)' nrd='0.29 / W' nrs='0.29 / W'
+ sa=0 sb=0 sd=0 mult=1 m=1
XMg20_11 s control v v sky130_fd_pr__pfet_01v8 L=2 W=1 nf=1 ad='int((nf+1)/2) * W/nf * 0.29' as='int((nf+2)/2) * W/nf * 0.29'
+ pd='2*int((nf+1)/2) * (W/nf + 0.29)' ps='2*int((nf+2)/2) * (W/nf + 0.29)' nrd='0.29 / W' nrs='0.29 / W'
+ sa=0 sb=0 sd=0 mult=1 m=1
XMg20_12 s control v v sky130_fd_pr__pfet_01v8 L=2 W=1 nf=1 ad='int((nf+1)/2) * W/nf * 0.29' as='int((nf+2)/2) * W/nf * 0.29'
+ pd='2*int((nf+1)/2) * (W/nf + 0.29)' ps='2*int((nf+2)/2) * (W/nf + 0.29)' nrd='0.29 / W' nrs='0.29 / W'
+ sa=0 sb=0 sd=0 mult=1 m=1
XMg20_13 s control v v sky130_fd_pr__pfet_01v8 L=2 W=1 nf=1 ad='int((nf+1)/2) * W/nf * 0.29' as='int((nf+2)/2) * W/nf * 0.29'
+ pd='2*int((nf+1)/2) * (W/nf + 0.29)' ps='2*int((nf+2)/2) * (W/nf + 0.29)' nrd='0.29 / W' nrs='0.29 / W'
+ sa=0 sb=0 sd=0 mult=1 m=1
XMg20_14 s control v v sky130_fd_pr__pfet_01v8 L=2 W=1 nf=1 ad='int((nf+1)/2) * W/nf * 0.29' as='int((nf+2)/2) * W/nf * 0.29'
+ pd='2*int((nf+1)/2) * (W/nf + 0.29)' ps='2*int((nf+2)/2) * (W/nf + 0.29)' nrd='0.29 / W' nrs='0.29 / W'
+ sa=0 sb=0 sd=0 mult=1 m=1
XMg20_15 s control v v sky130_fd_pr__pfet_01v8 L=2 W=1 nf=1 ad='int((nf+1)/2) * W/nf * 0.29' as='int((nf+2)/2) * W/nf * 0.29'
+ pd='2*int((nf+1)/2) * (W/nf + 0.29)' ps='2*int((nf+2)/2) * (W/nf + 0.29)' nrd='0.29 / W' nrs='0.29 / W'
+ sa=0 sb=0 sd=0 mult=1 m=1
XMg20_16 s control v v sky130_fd_pr__pfet_01v8 L=2 W=1 nf=1 ad='int((nf+1)/2) * W/nf * 0.29' as='int((nf+2)/2) * W/nf * 0.29'
+ pd='2*int((nf+1)/2) * (W/nf + 0.29)' ps='2*int((nf+2)/2) * (W/nf + 0.29)' nrd='0.29 / W' nrs='0.29 / W'
+ sa=0 sb=0 sd=0 mult=1 m=1
XMg20_17 s control v v sky130_fd_pr__pfet_01v8 L=2 W=1 nf=1 ad='int((nf+1)/2) * W/nf * 0.29' as='int((nf+2)/2) * W/nf * 0.29'
+ pd='2*int((nf+1)/2) * (W/nf + 0.29)' ps='2*int((nf+2)/2) * (W/nf + 0.29)' nrd='0.29 / W' nrs='0.29 / W'
+ sa=0 sb=0 sd=0 mult=1 m=1
XMg20_18 s control v v sky130_fd_pr__pfet_01v8 L=2 W=1 nf=1 ad='int((nf+1)/2) * W/nf * 0.29' as='int((nf+2)/2) * W/nf * 0.29'
+ pd='2*int((nf+1)/2) * (W/nf + 0.29)' ps='2*int((nf+2)/2) * (W/nf + 0.29)' nrd='0.29 / W' nrs='0.29 / W'
+ sa=0 sb=0 sd=0 mult=1 m=1
XMg20_19 s control v v sky130_fd_pr__pfet_01v8 L=2 W=1 nf=1 ad='int((nf+1)/2) * W/nf * 0.29' as='int((nf+2)/2) * W/nf * 0.29'
+ pd='2*int((nf+1)/2) * (W/nf + 0.29)' ps='2*int((nf+2)/2) * (W/nf + 0.29)' nrd='0.29 / W' nrs='0.29 / W'
+ sa=0 sb=0 sd=0 mult=1 m=1
XMg20_20 s control v v sky130_fd_pr__pfet_01v8 L=2 W=1 nf=1 ad='int((nf+1)/2) * W/nf * 0.29' as='int((nf+2)/2) * W/nf * 0.29'
+ pd='2*int((nf+1)/2) * (W/nf + 0.29)' ps='2*int((nf+2)/2) * (W/nf + 0.29)' nrd='0.29 / W' nrs='0.29 / W'
+ sa=0 sb=0 sd=0 mult=1 m=1
.ends


* expanding   symbol:  bank.sym # of pins=33
** sym_path: review/xschem/bank.sym
** sch_path: review/xschem/bank.sch
.subckt bank rail well g oa0 ob0 oa1 ob1 oa2 ob2 oa3 ob3 oa4 ob4 oa5 ob5 oa6 ob6 oa7 ob7 oa8 ob8 oa9
+ ob9 oa10 ob10 oa11 ob11 oa12 ob12 oa13 ob13 oa14 ob14
*.iopin rail
*.iopin well
*.iopin g
*.iopin oa0
*.iopin ob0
*.iopin oa1
*.iopin ob1
*.iopin oa2
*.iopin ob2
*.iopin oa3
*.iopin ob3
*.iopin oa4
*.iopin ob4
*.iopin oa5
*.iopin ob5
*.iopin oa6
*.iopin ob6
*.iopin oa7
*.iopin ob7
*.iopin oa8
*.iopin ob8
*.iopin oa9
*.iopin ob9
*.iopin oa10
*.iopin ob10
*.iopin oa11
*.iopin ob11
*.iopin oa12
*.iopin ob12
*.iopin oa13
*.iopin ob13
*.iopin oa14
*.iopin ob14
X0 oa14 ob14 oa0 ob0 rail g well stage
X1 oa0 ob0 oa1 ob1 rail g well stage
X2 oa1 ob1 oa2 ob2 rail g well stage
X3 oa2 ob2 oa3 ob3 rail g well stage
X4 oa3 ob3 oa4 ob4 rail g well stage
X5 oa4 ob4 oa5 ob5 rail g well stage
X6 oa5 ob5 oa6 ob6 rail g well stage
X7 oa6 ob6 oa7 ob7 rail g well stage
X8 oa7 ob7 oa8 ob8 rail g well stage
X9 oa8 ob8 oa9 ob9 rail g well stage
X10 oa9 ob9 oa10 ob10 rail g well stage
X11 oa10 ob10 oa11 ob11 rail g well stage
X12 oa11 ob11 oa12 ob12 rail g well stage
X13 oa12 ob12 oa13 ob13 rail g well stage
X14 oa13 ob13 oa14 ob14 rail g well stage
Xdummy well well dy dz g g well stage
.ends


* expanding   symbol:  cvsl.sym # of pins=5
** sym_path: review/xschem/cvsl.sym
** sch_path: review/xschem/cvsl.sch
.subckt cvsl a b out v g
*.iopin a
*.iopin b
*.iopin out
*.iopin v
*.iopin g
XMn0 l a g g sky130_fd_pr__nfet_01v8_lvt L=.15 W=4 nf=1 ad=1.16 as=1.16 pd=8.58 ps=8.58 nrd='0.29 / 4 '
+ nrs='0.29 / 4 ' sa=0 sb=0 sd=0 mult=1 m=1
XMn1 r b g g sky130_fd_pr__nfet_01v8_lvt L=.15 W=4 nf=1 ad=1.16 as=1.16 pd=8.58 ps=8.58 nrd='0.29 / 4 '
+ nrs='0.29 / 4 ' sa=0 sb=0 sd=0 mult=1 m=1
XMp0 l r v v sky130_fd_pr__pfet_01v8 L=2.4 W=.42 nf=1 ad=.122 as=.122 pd=1.42 ps=1.42 nrd='0.29 / W'
+ nrs='0.29 / W' sa=0 sb=0 sd=0 mult=1 m=1
XMp1 r l v v sky130_fd_pr__pfet_01v8 L=2.4 W=.42 nf=1 ad=.122 as=.122 pd=1.42 ps=1.42 nrd='0.29 / W'
+ nrs='0.29 / W' sa=0 sb=0 sd=0 mult=1 m=1
XMbuf_p out l v v sky130_fd_pr__pfet_01v8 L=.15 W=.84 nf=1 ad='int((nf+1)/2) * W/nf * 0.29' as='int((nf+2)/2) * W/nf * 0.29'
+ pd='2*int((nf+1)/2) * (W/nf + 0.29)' ps='2*int((nf+2)/2) * (W/nf + 0.29)' nrd='0.29 / W' nrs='0.29 / W'
+ sa=0 sb=0 sd=0 mult=1 m=1
XMbuf_n out l g g sky130_fd_pr__nfet_01v8 L=.15 W=.42 nf=1 ad='int((1 + 1)/2) * .42 / 1 * 0.29' as='int((1 + 2)/2) * .42 / 1 * 0.29'
+ pd='2*int((1 + 1)/2) * (.42 / 1 + 0.29)' ps='2*int((1 + 2)/2) * (.42 / 1 + 0.29)' nrd='0.29 / .42 ' nrs='0.29 / .42 '
+ sa=0 sb=0 sd=0 mult=1 m=1
XMdummy_p dummy r v v sky130_fd_pr__pfet_01v8 L=.15 W=.84 nf=1 ad='int((nf+1)/2) * W/nf * 0.29' as='int((nf+2)/2) * W/nf * 0.29'
+ pd='2*int((nf+1)/2) * (W/nf + 0.29)' ps='2*int((nf+2)/2) * (W/nf + 0.29)' nrd='0.29 / W' nrs='0.29 / W'
+ sa=0 sb=0 sd=0 mult=1 m=1
XMdummy_n dummy r g g sky130_fd_pr__nfet_01v8 L=.15 W=.42 nf=1 ad='int((1 + 1)/2) * .42 / 1 * 0.29' as='int((1 + 2)/2) * .42 / 1 * 0.29'
+ pd='2*int((1 + 1)/2) * (.42 / 1 + 0.29)' ps='2*int((1 + 2)/2) * (.42 / 1 + 0.29)' nrd='0.29 / .42 ' nrs='0.29 / .42 '
+ sa=0 sb=0 sd=0 mult=1 m=1
.ends


* expanding   symbol:  stage.sym # of pins=7
** sym_path: review/xschem/stage.sym
** sch_path: review/xschem/stage.sch
.subckt stage a b y z rail g well
*.iopin a
*.iopin b
*.iopin y
*.iopin z
*.iopin rail
*.iopin g
*.iopin well
XCca g y sky130_fd_pr__cap_mim_m3_1 W=4.5 L=4.5 MF=1 m=1
XCcb g z sky130_fd_pr__cap_mim_m3_1 W=4.5 L=4.5 MF=1 m=1
XMmainA_Xp y a rail well sky130_fd_pr__pfet_01v8_lvt L=.55 W=8.4 nf=1 ad='int((1 + 1)/2) * 8.4 / 1 * 0.29'
+ as='int((1 + 2)/2) * 8.4 / 1 * 0.29' pd='2*int((1 + 1)/2) * (8.4 / 1 + 0.29)' ps='2*int((1 + 2)/2) * (8.4 / 1 + 0.29)'
+ nrd='0.29 / 8.4 ' nrs='0.29 / 8.4 ' sa=0 sb=0 sd=0 mult=1 m=1
XMmainA_Xn y a g g sky130_fd_pr__nfet_01v8 L=.55 W=4.2 nf=1 ad='int((1 + 1)/2) * 4.2 / 1 * 0.29' as='int((1 + 2)/2) * 4.2 / 1 * 0.29'
+ pd='2*int((1 + 1)/2) * (4.2 / 1 + 0.29)' ps='2*int((1 + 2)/2) * (4.2 / 1 + 0.29)' nrd='0.29 / 4.2 ' nrs='0.29 / 4.2 '
+ sa=0 sb=0 sd=0 mult=1 m=1
XMmainB_Xp z b rail well sky130_fd_pr__pfet_01v8_lvt L=.55 W=8.4 nf=1 ad='int((1 + 1)/2) * 8.4 / 1 * 0.29'
+ as='int((1 + 2)/2) * 8.4 / 1 * 0.29' pd='2*int((1 + 1)/2) * (8.4 / 1 + 0.29)' ps='2*int((1 + 2)/2) * (8.4 / 1 + 0.29)'
+ nrd='0.29 / 8.4 ' nrs='0.29 / 8.4 ' sa=0 sb=0 sd=0 mult=1 m=1
XMmainB_Xn z b g g sky130_fd_pr__nfet_01v8 L=.55 W=4.2 nf=1 ad='int((1 + 1)/2) * 4.2 / 1 * 0.29' as='int((1 + 2)/2) * 4.2 / 1 * 0.29'
+ pd='2*int((1 + 1)/2) * (4.2 / 1 + 0.29)' ps='2*int((1 + 2)/2) * (4.2 / 1 + 0.29)' nrd='0.29 / 4.2 ' nrs='0.29 / 4.2 '
+ sa=0 sb=0 sd=0 mult=1 m=1
XMcrossA_Xp z y rail well sky130_fd_pr__pfet_01v8_lvt L=.55 W=1.68 nf=1 ad='int((1 + 1)/2) * 1.68 / 1 * 0.29'
+ as='int((1 + 2)/2) * 1.68 / 1 * 0.29' pd='2*int((1 + 1)/2) * (1.68 / 1 + 0.29)' ps='2*int((1 + 2)/2) * (1.68 / 1 + 0.29)'
+ nrd='0.29 / 1.68 ' nrs='0.29 / 1.68 ' sa=0 sb=0 sd=0 mult=1 m=1
XMcrossA_Xn z y g g sky130_fd_pr__nfet_01v8 L=.55 W=.84 nf=1 ad='int((1 + 1)/2) * .84 / 1 * 0.29' as='int((1 + 2)/2) * .84 / 1 * 0.29'
+ pd='2*int((1 + 1)/2) * (.84 / 1 + 0.29)' ps='2*int((1 + 2)/2) * (.84 / 1 + 0.29)' nrd='0.29 / .84 ' nrs='0.29 / .84 '
+ sa=0 sb=0 sd=0 mult=1 m=1
XMcrossB_Xp y z rail well sky130_fd_pr__pfet_01v8_lvt L=.55 W=1.68 nf=1 ad='int((1 + 1)/2) * 1.68 / 1 * 0.29'
+ as='int((1 + 2)/2) * 1.68 / 1 * 0.29' pd='2*int((1 + 1)/2) * (1.68 / 1 + 0.29)' ps='2*int((1 + 2)/2) * (1.68 / 1 + 0.29)'
+ nrd='0.29 / 1.68 ' nrs='0.29 / 1.68 ' sa=0 sb=0 sd=0 mult=1 m=1
XMcrossB_Xn y z g g sky130_fd_pr__nfet_01v8 L=.55 W=.84 nf=1 ad='int((1 + 1)/2) * .84 / 1 * 0.29' as='int((1 + 2)/2) * .84 / 1 * 0.29'
+ pd='2*int((1 + 1)/2) * (.84 / 1 + 0.29)' ps='2*int((1 + 2)/2) * (.84 / 1 + 0.29)' nrd='0.29 / .84 ' nrs='0.29 / .84 '
+ sa=0 sb=0 sd=0 mult=1 m=1
.ends

.end
